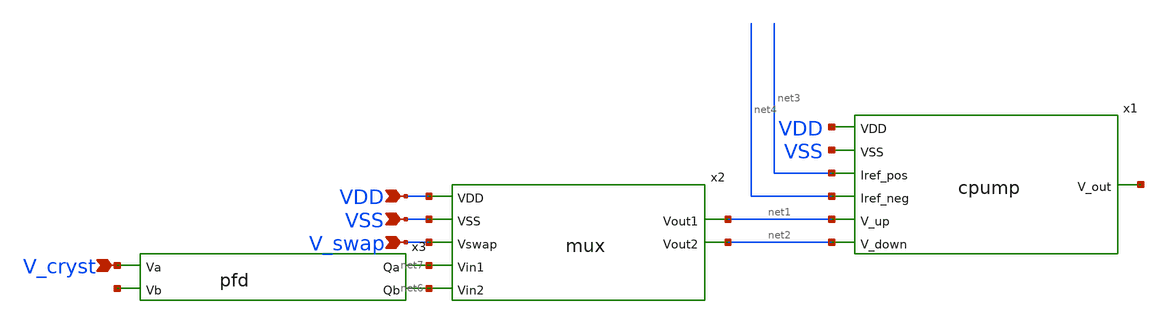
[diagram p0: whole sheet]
** sch_path: blocks/pll/pll.sch
**.subckt pll VDD VSS V_swap V_cryst
*.ipin VDD
*.ipin VSS
*.ipin V_swap
*.ipin V_cryst
x1 net3 VDD net1 net5 net2 VSS net4 cpump
x2 net2 net6 VDD V_swap VSS net1 net7 mux
x3 V_cryst net7 net8 net6 pfd
**.ends
.end
